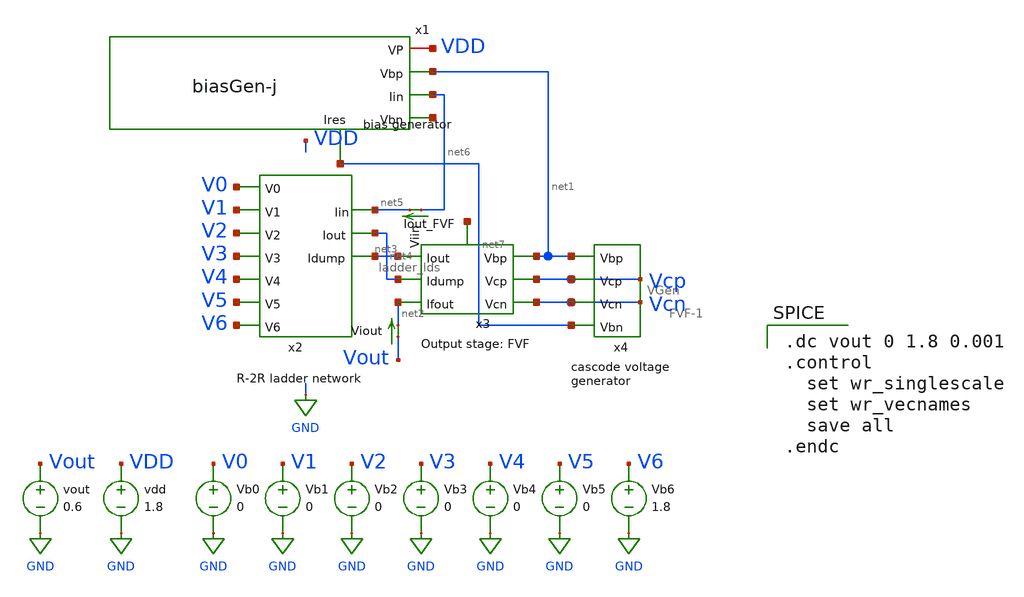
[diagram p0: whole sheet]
** sch_path: xschem/new_sim_cascode_supply_sweep_ladder_lds.sch
**.subckt new_sim_cascode_supply_sweep_ladder_lds
Vb1 V1 GND 0
Vb2 V2 GND 0
Vb3 V3 GND 0
Vb4 V4 GND 0
Vb5 V5 GND 0
Vb6 V6 GND 1.8
Vb0 V0 GND 0
x3 net1 Vcp net3 Vcn net2 net4 net8 FVF-1
x4 net1 Vcn Vcp net7 VGen
vdd VDD GND 1.8
vout Vout GND 0.6
Viout Vout net2 0
.save i(viout)
Viin net6 net5 0
.save i(viin)
x1 VDD net1 net6 net9 net7 biasGen-j
x2 V0 net3 net4 net5 V1 V2 V3 V4 V5 V6 ladder_lds
**** begin user architecture code

.option wnflag=1
.param MC_SWITCH=0.0
.lib ~/skywater/skywater-pdk/libraries/sky130_fd_pr_ngspice/latest/models/sky130.lib.spice tt


.dc vout 0 1.8 0.001
.control
  set wr_singlescale
  set wr_vecnames
  save all
.endc

**** end user architecture code
**.ends
.GLOBAL GND
.end
